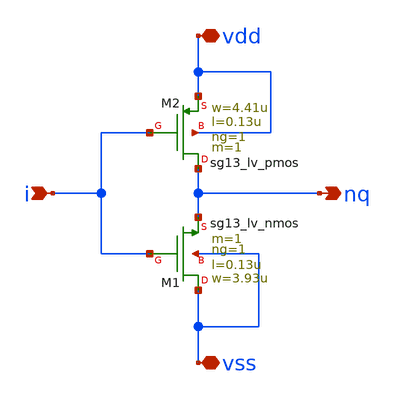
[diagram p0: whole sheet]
** sch_path: ihp-sg13g2/libs.ref/sg13g2_io/xschem/sg13g2_io_inv_x1.sch
**.subckt sg13g2_io_inv_x1 i vdd vss nq
*.ipin i
*.iopin vdd
*.iopin vss
*.opin nq
XM2 nq i vdd vdd sg13_lv_pmos w=4.41u l=0.13u ng=1 m=1 mm_ok=1
XM1 vss i nq vss sg13_lv_nmos w=3.93u l=0.13u ng=1 m=1 mm_ok=1
**.ends
.end
